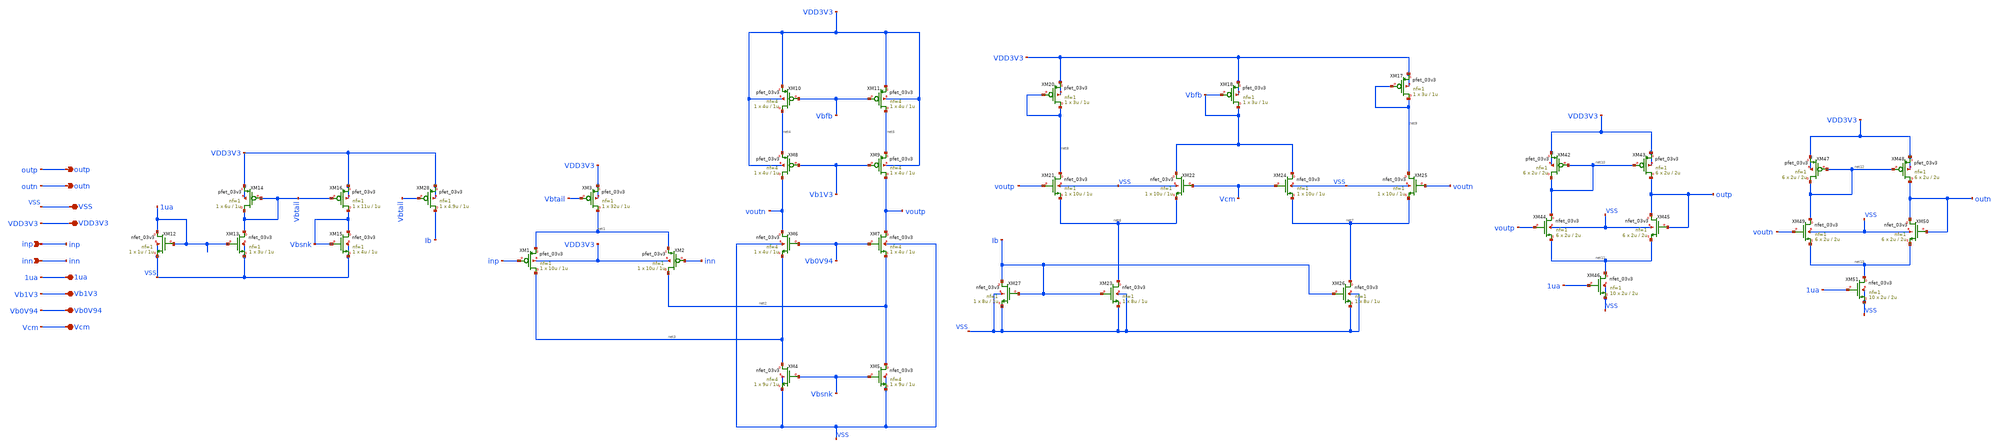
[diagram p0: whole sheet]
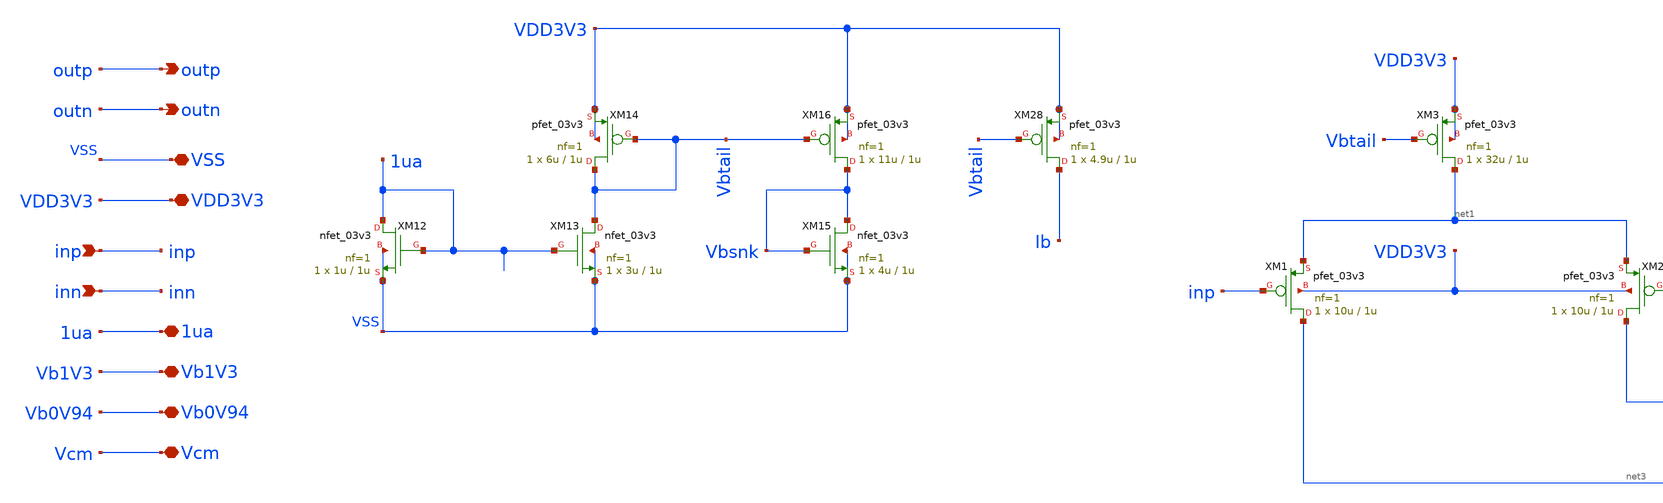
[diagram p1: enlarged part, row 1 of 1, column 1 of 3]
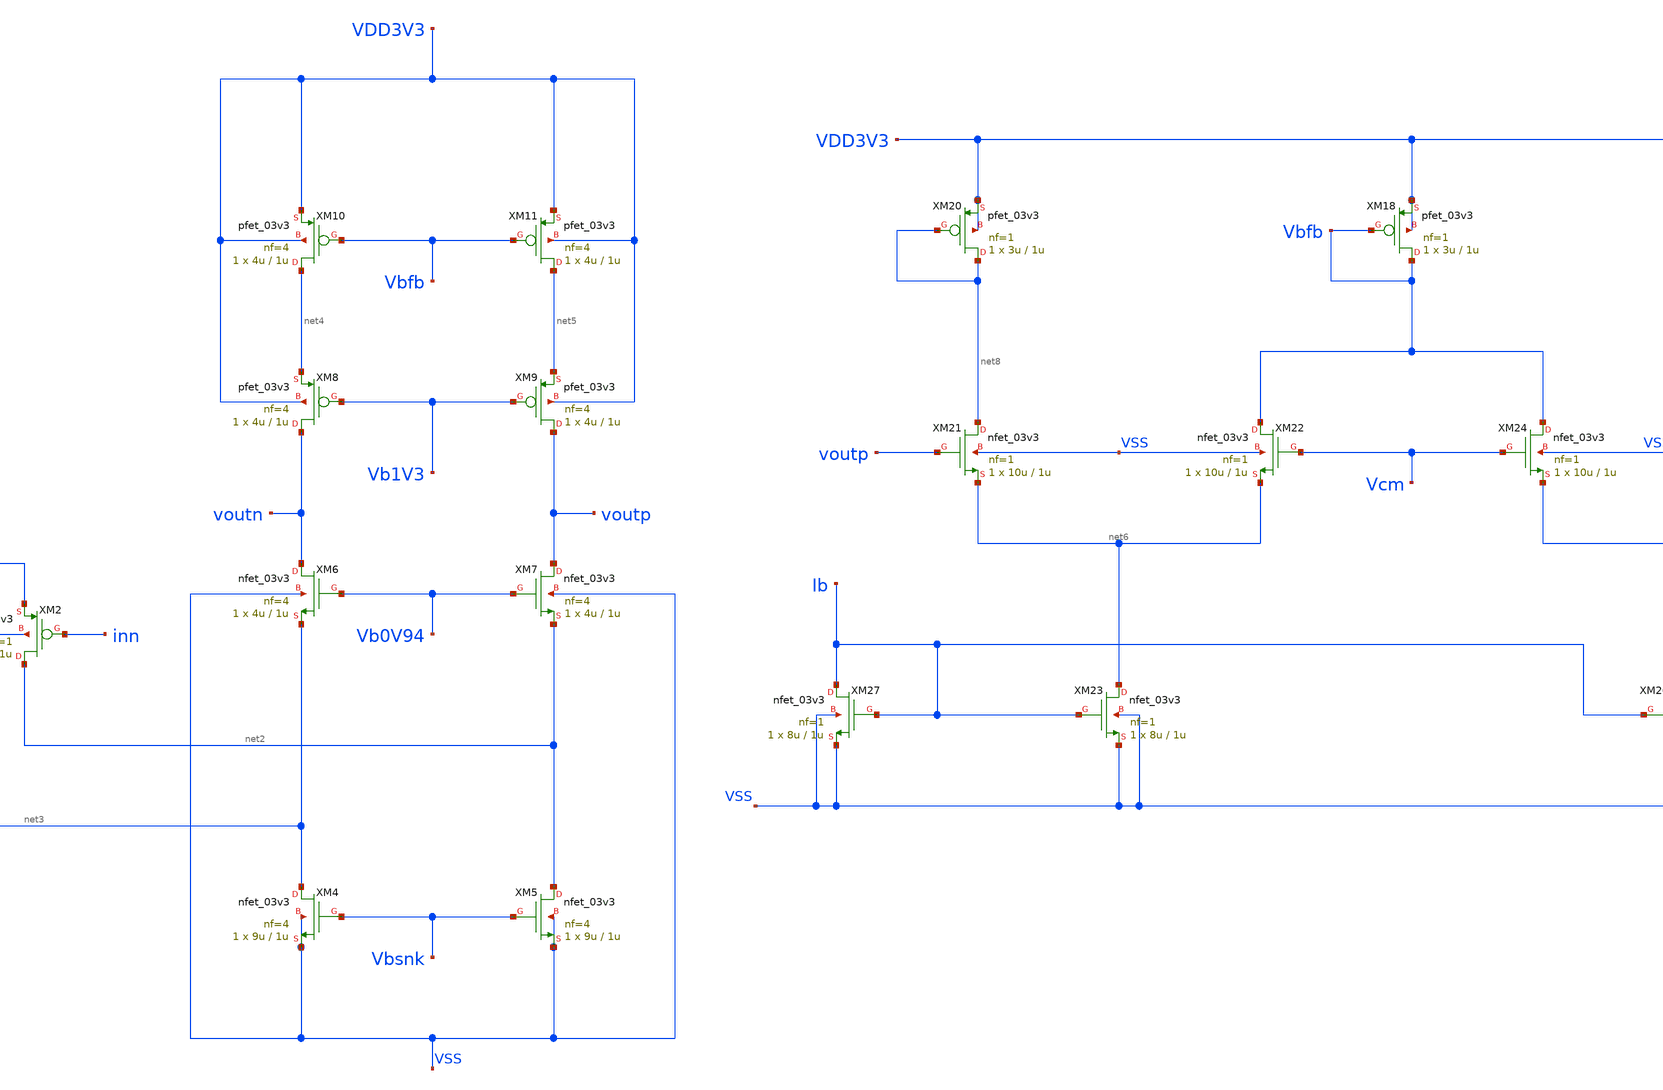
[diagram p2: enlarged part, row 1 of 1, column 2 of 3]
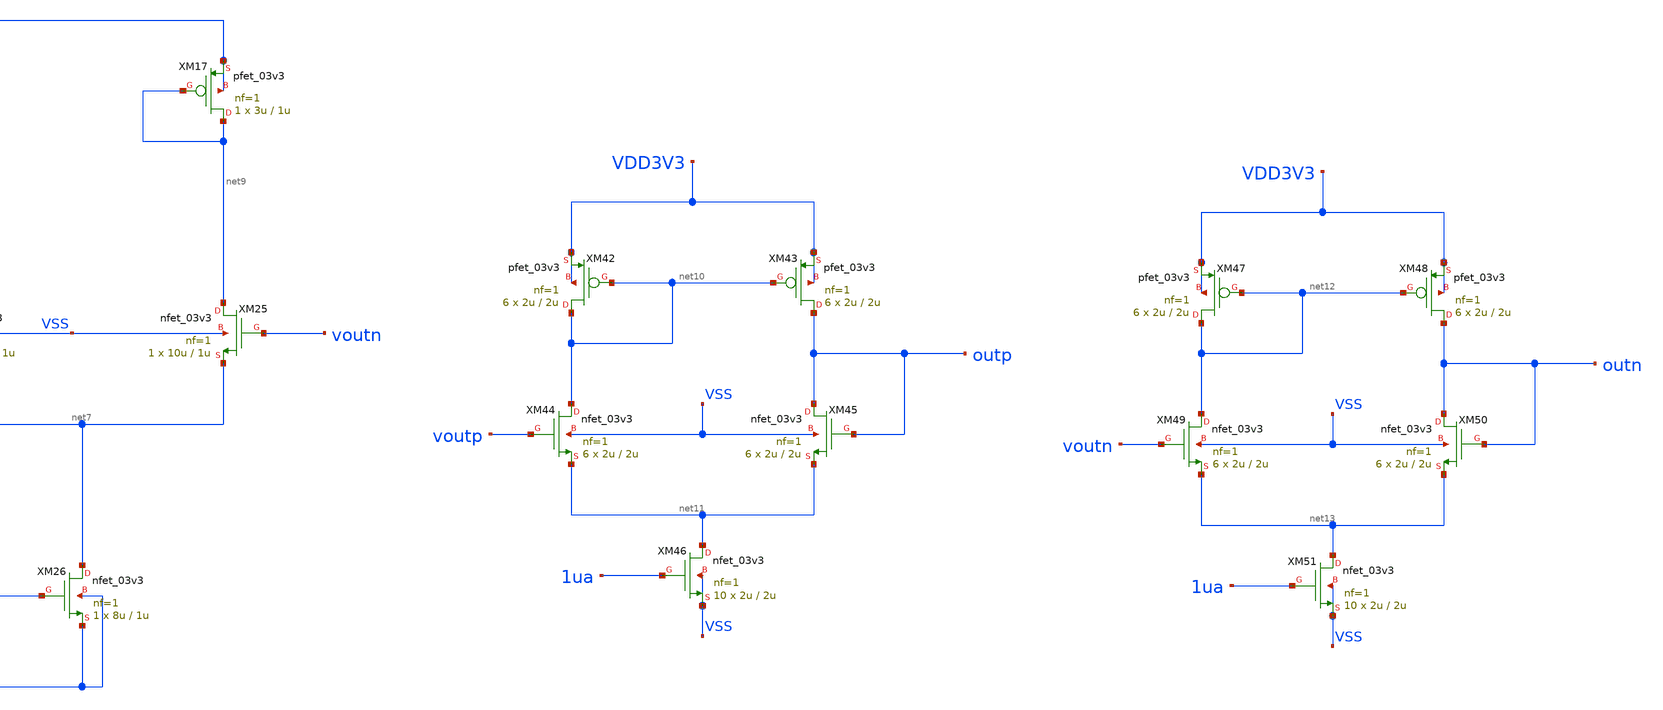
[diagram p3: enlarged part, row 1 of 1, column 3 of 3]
** sch_path: designs/libs/core_pga/folded_cascode/folded_cascode_v2.sch
**.subckt folded_cascode_v2 outp outn VSS VDD3V3 inp inn 1ua Vb1V3 Vb0V94 Vcm
*.opin outp
*.opin outn
*.iopin VSS
*.iopin VDD3V3
*.ipin inp
*.ipin inn
*.iopin 1ua
*.iopin Vb1V3
*.iopin Vb0V94
*.iopin Vcm
XM1 net3 inp net1 VDD3V3 pfet_03v3 L=1u W=10u nf=1 ad='int((nf+1)/2) * W/nf * 0.18u' as='int((nf+2)/2) * W/nf * 0.18u'
+ pd='2*int((nf+1)/2) * (W/nf + 0.18u)' ps='2*int((nf+2)/2) * (W/nf + 0.18u)' nrd='0.18u / W' nrs='0.18u / W'
+ sa=0 sb=0 sd=0 m=1
XM2 net2 inn net1 VDD3V3 pfet_03v3 L=1u W=10u nf=1 ad='int((nf+1)/2) * W/nf * 0.18u' as='int((nf+2)/2) * W/nf * 0.18u'
+ pd='2*int((nf+1)/2) * (W/nf + 0.18u)' ps='2*int((nf+2)/2) * (W/nf + 0.18u)' nrd='0.18u / W' nrs='0.18u / W'
+ sa=0 sb=0 sd=0 m=1
XM6 voutn Vb0V94 net3 VSS nfet_03v3 L=1u W=4u nf=4 ad='int((nf+1)/2) * W/nf * 0.18u' as='int((nf+2)/2) * W/nf * 0.18u'
+ pd='2*int((nf+1)/2) * (W/nf + 0.18u)' ps='2*int((nf+2)/2) * (W/nf + 0.18u)' nrd='0.18u / W' nrs='0.18u / W'
+ sa=0 sb=0 sd=0 m=1
XM7 voutp Vb0V94 net2 VSS nfet_03v3 L=1u W=4u nf=4 ad='int((nf+1)/2) * W/nf * 0.18u' as='int((nf+2)/2) * W/nf * 0.18u'
+ pd='2*int((nf+1)/2) * (W/nf + 0.18u)' ps='2*int((nf+2)/2) * (W/nf + 0.18u)' nrd='0.18u / W' nrs='0.18u / W'
+ sa=0 sb=0 sd=0 m=1
XM8 voutn Vb1V3 net4 VDD3V3 pfet_03v3 L=1u W=4u nf=4 ad='int((nf+1)/2) * W/nf * 0.18u' as='int((nf+2)/2) * W/nf * 0.18u'
+ pd='2*int((nf+1)/2) * (W/nf + 0.18u)' ps='2*int((nf+2)/2) * (W/nf + 0.18u)' nrd='0.18u / W' nrs='0.18u / W'
+ sa=0 sb=0 sd=0 m=1
XM9 voutp Vb1V3 net5 VDD3V3 pfet_03v3 L=1u W=4u nf=4 ad='int((nf+1)/2) * W/nf * 0.18u' as='int((nf+2)/2) * W/nf * 0.18u'
+ pd='2*int((nf+1)/2) * (W/nf + 0.18u)' ps='2*int((nf+2)/2) * (W/nf + 0.18u)' nrd='0.18u / W' nrs='0.18u / W'
+ sa=0 sb=0 sd=0 m=1
XM3 net1 Vbtail VDD3V3 VDD3V3 pfet_03v3 L=1u W=32u nf=1 ad='int((nf+1)/2) * W/nf * 0.18u' as='int((nf+2)/2) * W/nf * 0.18u'
+ pd='2*int((nf+1)/2) * (W/nf + 0.18u)' ps='2*int((nf+2)/2) * (W/nf + 0.18u)' nrd='0.18u / W' nrs='0.18u / W'
+ sa=0 sb=0 sd=0 m=1
XM4 net3 Vbsnk VSS VSS nfet_03v3 L=1u W=9u nf=4 ad='int((nf+1)/2) * W/nf * 0.18u' as='int((nf+2)/2) * W/nf * 0.18u'
+ pd='2*int((nf+1)/2) * (W/nf + 0.18u)' ps='2*int((nf+2)/2) * (W/nf + 0.18u)' nrd='0.18u / W' nrs='0.18u / W'
+ sa=0 sb=0 sd=0 m=1
XM5 net2 Vbsnk VSS VSS nfet_03v3 L=1u W=9u nf=4 ad='int((nf+1)/2) * W/nf * 0.18u' as='int((nf+2)/2) * W/nf * 0.18u'
+ pd='2*int((nf+1)/2) * (W/nf + 0.18u)' ps='2*int((nf+2)/2) * (W/nf + 0.18u)' nrd='0.18u / W' nrs='0.18u / W'
+ sa=0 sb=0 sd=0 m=1
XM10 net4 Vbfb VDD3V3 VDD3V3 pfet_03v3 L=1u W=4u nf=4 ad='int((nf+1)/2) * W/nf * 0.18u' as='int((nf+2)/2) * W/nf * 0.18u'
+ pd='2*int((nf+1)/2) * (W/nf + 0.18u)' ps='2*int((nf+2)/2) * (W/nf + 0.18u)' nrd='0.18u / W' nrs='0.18u / W'
+ sa=0 sb=0 sd=0 m=1
XM11 net5 Vbfb VDD3V3 VDD3V3 pfet_03v3 L=1u W=4u nf=4 ad='int((nf+1)/2) * W/nf * 0.18u' as='int((nf+2)/2) * W/nf * 0.18u'
+ pd='2*int((nf+1)/2) * (W/nf + 0.18u)' ps='2*int((nf+2)/2) * (W/nf + 0.18u)' nrd='0.18u / W' nrs='0.18u / W'
+ sa=0 sb=0 sd=0 m=1
XM20 net8 net8 VDD3V3 VDD3V3 pfet_03v3 L=1u W=3u nf=1 ad='int((nf+1)/2) * W/nf * 0.18u' as='int((nf+2)/2) * W/nf * 0.18u'
+ pd='2*int((nf+1)/2) * (W/nf + 0.18u)' ps='2*int((nf+2)/2) * (W/nf + 0.18u)' nrd='0.18u / W' nrs='0.18u / W'
+ sa=0 sb=0 sd=0 m=1
XM21 net8 voutp net6 VSS nfet_03v3 L=1u W=10u nf=1 ad='int((nf+1)/2) * W/nf * 0.18u' as='int((nf+2)/2) * W/nf * 0.18u'
+ pd='2*int((nf+1)/2) * (W/nf + 0.18u)' ps='2*int((nf+2)/2) * (W/nf + 0.18u)' nrd='0.18u / W' nrs='0.18u / W'
+ sa=0 sb=0 sd=0 m=1
XM22 Vbfb Vcm net6 VSS nfet_03v3 L=1u W=10u nf=1 ad='int((nf+1)/2) * W/nf * 0.18u' as='int((nf+2)/2) * W/nf * 0.18u'
+ pd='2*int((nf+1)/2) * (W/nf + 0.18u)' ps='2*int((nf+2)/2) * (W/nf + 0.18u)' nrd='0.18u / W' nrs='0.18u / W'
+ sa=0 sb=0 sd=0 m=1
XM23 net6 Ib VSS VSS nfet_03v3 L=1u W=8u nf=1 ad='int((nf+1)/2) * W/nf * 0.18u' as='int((nf+2)/2) * W/nf * 0.18u'
+ pd='2*int((nf+1)/2) * (W/nf + 0.18u)' ps='2*int((nf+2)/2) * (W/nf + 0.18u)' nrd='0.18u / W' nrs='0.18u / W'
+ sa=0 sb=0 sd=0 m=1
XM24 Vbfb Vcm net7 VSS nfet_03v3 L=1u W=10u nf=1 ad='int((nf+1)/2) * W/nf * 0.18u' as='int((nf+2)/2) * W/nf * 0.18u'
+ pd='2*int((nf+1)/2) * (W/nf + 0.18u)' ps='2*int((nf+2)/2) * (W/nf + 0.18u)' nrd='0.18u / W' nrs='0.18u / W'
+ sa=0 sb=0 sd=0 m=1
XM25 net9 voutn net7 VSS nfet_03v3 L=1u W=10u nf=1 ad='int((nf+1)/2) * W/nf * 0.18u' as='int((nf+2)/2) * W/nf * 0.18u'
+ pd='2*int((nf+1)/2) * (W/nf + 0.18u)' ps='2*int((nf+2)/2) * (W/nf + 0.18u)' nrd='0.18u / W' nrs='0.18u / W'
+ sa=0 sb=0 sd=0 m=1
XM26 net7 Ib VSS VSS nfet_03v3 L=1u W=8u nf=1 ad='int((nf+1)/2) * W/nf * 0.18u' as='int((nf+2)/2) * W/nf * 0.18u'
+ pd='2*int((nf+1)/2) * (W/nf + 0.18u)' ps='2*int((nf+2)/2) * (W/nf + 0.18u)' nrd='0.18u / W' nrs='0.18u / W'
+ sa=0 sb=0 sd=0 m=1
XM27 Ib Ib VSS VSS nfet_03v3 L=1u W=8u nf=1 ad='int((nf+1)/2) * W/nf * 0.18u' as='int((nf+2)/2) * W/nf * 0.18u'
+ pd='2*int((nf+1)/2) * (W/nf + 0.18u)' ps='2*int((nf+2)/2) * (W/nf + 0.18u)' nrd='0.18u / W' nrs='0.18u / W'
+ sa=0 sb=0 sd=0 m=1
XM12 1ua 1ua VSS VSS nfet_03v3 L=1u W=1u nf=1 ad='int((nf+1)/2) * W/nf * 0.18u' as='int((nf+2)/2) * W/nf * 0.18u'
+ pd='2*int((nf+1)/2) * (W/nf + 0.18u)' ps='2*int((nf+2)/2) * (W/nf + 0.18u)' nrd='0.18u / W' nrs='0.18u / W'
+ sa=0 sb=0 sd=0 m=1
XM13 Vbtail 1ua VSS VSS nfet_03v3 L=1u W=3u nf=1 ad='int((nf+1)/2) * W/nf * 0.18u' as='int((nf+2)/2) * W/nf * 0.18u'
+ pd='2*int((nf+1)/2) * (W/nf + 0.18u)' ps='2*int((nf+2)/2) * (W/nf + 0.18u)' nrd='0.18u / W' nrs='0.18u / W'
+ sa=0 sb=0 sd=0 m=1
XM14 Vbtail Vbtail VDD3V3 VDD3V3 pfet_03v3 L=1u W=6u nf=1 ad='int((nf+1)/2) * W/nf * 0.18u' as='int((nf+2)/2) * W/nf * 0.18u'
+ pd='2*int((nf+1)/2) * (W/nf + 0.18u)' ps='2*int((nf+2)/2) * (W/nf + 0.18u)' nrd='0.18u / W' nrs='0.18u / W'
+ sa=0 sb=0 sd=0 m=1
XM15 Vbsnk Vbsnk VSS VSS nfet_03v3 L=1u W=4u nf=1 ad='int((nf+1)/2) * W/nf * 0.18u' as='int((nf+2)/2) * W/nf * 0.18u'
+ pd='2*int((nf+1)/2) * (W/nf + 0.18u)' ps='2*int((nf+2)/2) * (W/nf + 0.18u)' nrd='0.18u / W' nrs='0.18u / W'
+ sa=0 sb=0 sd=0 m=1
XM16 Vbsnk Vbtail VDD3V3 VDD3V3 pfet_03v3 L=1u W=11u nf=1 ad='int((nf+1)/2) * W/nf * 0.18u' as='int((nf+2)/2) * W/nf * 0.18u'
+ pd='2*int((nf+1)/2) * (W/nf + 0.18u)' ps='2*int((nf+2)/2) * (W/nf + 0.18u)' nrd='0.18u / W' nrs='0.18u / W'
+ sa=0 sb=0 sd=0 m=1
XM17 net9 net9 VDD3V3 VDD3V3 pfet_03v3 L=1u W=3u nf=1 ad='int((nf+1)/2) * W/nf * 0.18u' as='int((nf+2)/2) * W/nf * 0.18u'
+ pd='2*int((nf+1)/2) * (W/nf + 0.18u)' ps='2*int((nf+2)/2) * (W/nf + 0.18u)' nrd='0.18u / W' nrs='0.18u / W'
+ sa=0 sb=0 sd=0 m=1
XM18 Vbfb Vbfb VDD3V3 VDD3V3 pfet_03v3 L=1u W=3u nf=1 ad='int((nf+1)/2) * W/nf * 0.18u' as='int((nf+2)/2) * W/nf * 0.18u'
+ pd='2*int((nf+1)/2) * (W/nf + 0.18u)' ps='2*int((nf+2)/2) * (W/nf + 0.18u)' nrd='0.18u / W' nrs='0.18u / W'
+ sa=0 sb=0 sd=0 m=1
XM28 Ib Vbtail VDD3V3 VDD3V3 pfet_03v3 L=1u W=4.9u nf=1 ad='int((nf+1)/2) * W/nf * 0.18u' as='int((nf+2)/2) * W/nf * 0.18u'
+ pd='2*int((nf+1)/2) * (W/nf + 0.18u)' ps='2*int((nf+2)/2) * (W/nf + 0.18u)' nrd='0.18u / W' nrs='0.18u / W'
+ sa=0 sb=0 sd=0 m=1
XM42 net10 net10 VDD3V3 VDD3V3 pfet_03v3 L=2u W=2u nf=1 ad='int((nf+1)/2) * W/nf * 0.18u' as='int((nf+2)/2) * W/nf * 0.18u'
+ pd='2*int((nf+1)/2) * (W/nf + 0.18u)' ps='2*int((nf+2)/2) * (W/nf + 0.18u)' nrd='0.18u / W' nrs='0.18u / W'
+ sa=0 sb=0 sd=0 m=6
XM43 outp net10 VDD3V3 VDD3V3 pfet_03v3 L=2u W=2u nf=1 ad='int((nf+1)/2) * W/nf * 0.18u' as='int((nf+2)/2) * W/nf * 0.18u'
+ pd='2*int((nf+1)/2) * (W/nf + 0.18u)' ps='2*int((nf+2)/2) * (W/nf + 0.18u)' nrd='0.18u / W' nrs='0.18u / W'
+ sa=0 sb=0 sd=0 m=6
XM44 net10 voutp net11 VSS nfet_03v3 L=2u W=2u nf=1 ad='int((nf+1)/2) * W/nf * 0.18u' as='int((nf+2)/2) * W/nf * 0.18u'
+ pd='2*int((nf+1)/2) * (W/nf + 0.18u)' ps='2*int((nf+2)/2) * (W/nf + 0.18u)' nrd='0.18u / W' nrs='0.18u / W'
+ sa=0 sb=0 sd=0 m=6
XM45 outp outp net11 VSS nfet_03v3 L=2u W=2u nf=1 ad='int((nf+1)/2) * W/nf * 0.18u' as='int((nf+2)/2) * W/nf * 0.18u'
+ pd='2*int((nf+1)/2) * (W/nf + 0.18u)' ps='2*int((nf+2)/2) * (W/nf + 0.18u)' nrd='0.18u / W' nrs='0.18u / W'
+ sa=0 sb=0 sd=0 m=6
XM46 net11 1ua VSS VSS nfet_03v3 L=2u W=2u nf=1 ad='int((nf+1)/2) * W/nf * 0.18u' as='int((nf+2)/2) * W/nf * 0.18u'
+ pd='2*int((nf+1)/2) * (W/nf + 0.18u)' ps='2*int((nf+2)/2) * (W/nf + 0.18u)' nrd='0.18u / W' nrs='0.18u / W'
+ sa=0 sb=0 sd=0 m=10
XM47 net12 net12 VDD3V3 VDD3V3 pfet_03v3 L=2u W=2u nf=1 ad='int((nf+1)/2) * W/nf * 0.18u' as='int((nf+2)/2) * W/nf * 0.18u'
+ pd='2*int((nf+1)/2) * (W/nf + 0.18u)' ps='2*int((nf+2)/2) * (W/nf + 0.18u)' nrd='0.18u / W' nrs='0.18u / W'
+ sa=0 sb=0 sd=0 m=6
XM48 outn net12 VDD3V3 VDD3V3 pfet_03v3 L=2u W=2u nf=1 ad='int((nf+1)/2) * W/nf * 0.18u' as='int((nf+2)/2) * W/nf * 0.18u'
+ pd='2*int((nf+1)/2) * (W/nf + 0.18u)' ps='2*int((nf+2)/2) * (W/nf + 0.18u)' nrd='0.18u / W' nrs='0.18u / W'
+ sa=0 sb=0 sd=0 m=6
XM49 net12 voutn net13 VSS nfet_03v3 L=2u W=2u nf=1 ad='int((nf+1)/2) * W/nf * 0.18u' as='int((nf+2)/2) * W/nf * 0.18u'
+ pd='2*int((nf+1)/2) * (W/nf + 0.18u)' ps='2*int((nf+2)/2) * (W/nf + 0.18u)' nrd='0.18u / W' nrs='0.18u / W'
+ sa=0 sb=0 sd=0 m=6
XM50 outn outn net13 VSS nfet_03v3 L=2u W=2u nf=1 ad='int((nf+1)/2) * W/nf * 0.18u' as='int((nf+2)/2) * W/nf * 0.18u'
+ pd='2*int((nf+1)/2) * (W/nf + 0.18u)' ps='2*int((nf+2)/2) * (W/nf + 0.18u)' nrd='0.18u / W' nrs='0.18u / W'
+ sa=0 sb=0 sd=0 m=6
XM51 net13 1ua VSS VSS nfet_03v3 L=2u W=2u nf=1 ad='int((nf+1)/2) * W/nf * 0.18u' as='int((nf+2)/2) * W/nf * 0.18u'
+ pd='2*int((nf+1)/2) * (W/nf + 0.18u)' ps='2*int((nf+2)/2) * (W/nf + 0.18u)' nrd='0.18u / W' nrs='0.18u / W'
+ sa=0 sb=0 sd=0 m=10
**.ends
.end
